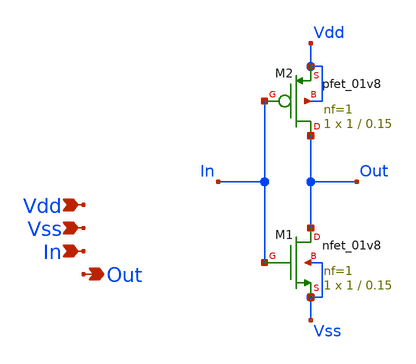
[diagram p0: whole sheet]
** sch_path: xschem/T0/inv/inv.sch
**.subckt inv Vdd Vss Out In
*.ipin Vdd
*.ipin Vss
*.opin Out
*.ipin In
XM1 Out In Vss Vss sky130_fd_pr__nfet_01v8 L=0.15 W=1 nf=1 ad='int((1 + 1)/2) * 1 / 1 * 0.29' as='int((1 + 2)/2) * 1 / 1 * 0.29'
+ pd='2*int((1 + 1)/2) * (1 / 1 + 0.29)' ps='2*int((1 + 2)/2) * (1 / 1 + 0.29)' nrd='0.29 / 1 ' nrs='0.29 / 1 '
+ sa=0 sb=0 sd=0 mult=1 m=1
XM2 Out In Vdd Vdd sky130_fd_pr__pfet_01v8 L=0.15 W=1 nf=1 ad='int((nf+1)/2) * W/nf * 0.29' as='int((nf+2)/2) * W/nf * 0.29'
+ pd='2*int((nf+1)/2) * (W/nf + 0.29)' ps='2*int((nf+2)/2) * (W/nf + 0.29)' nrd='0.29 / W' nrs='0.29 / W'
+ sa=0 sb=0 sd=0 mult=1 m=1
**.ends
.end
